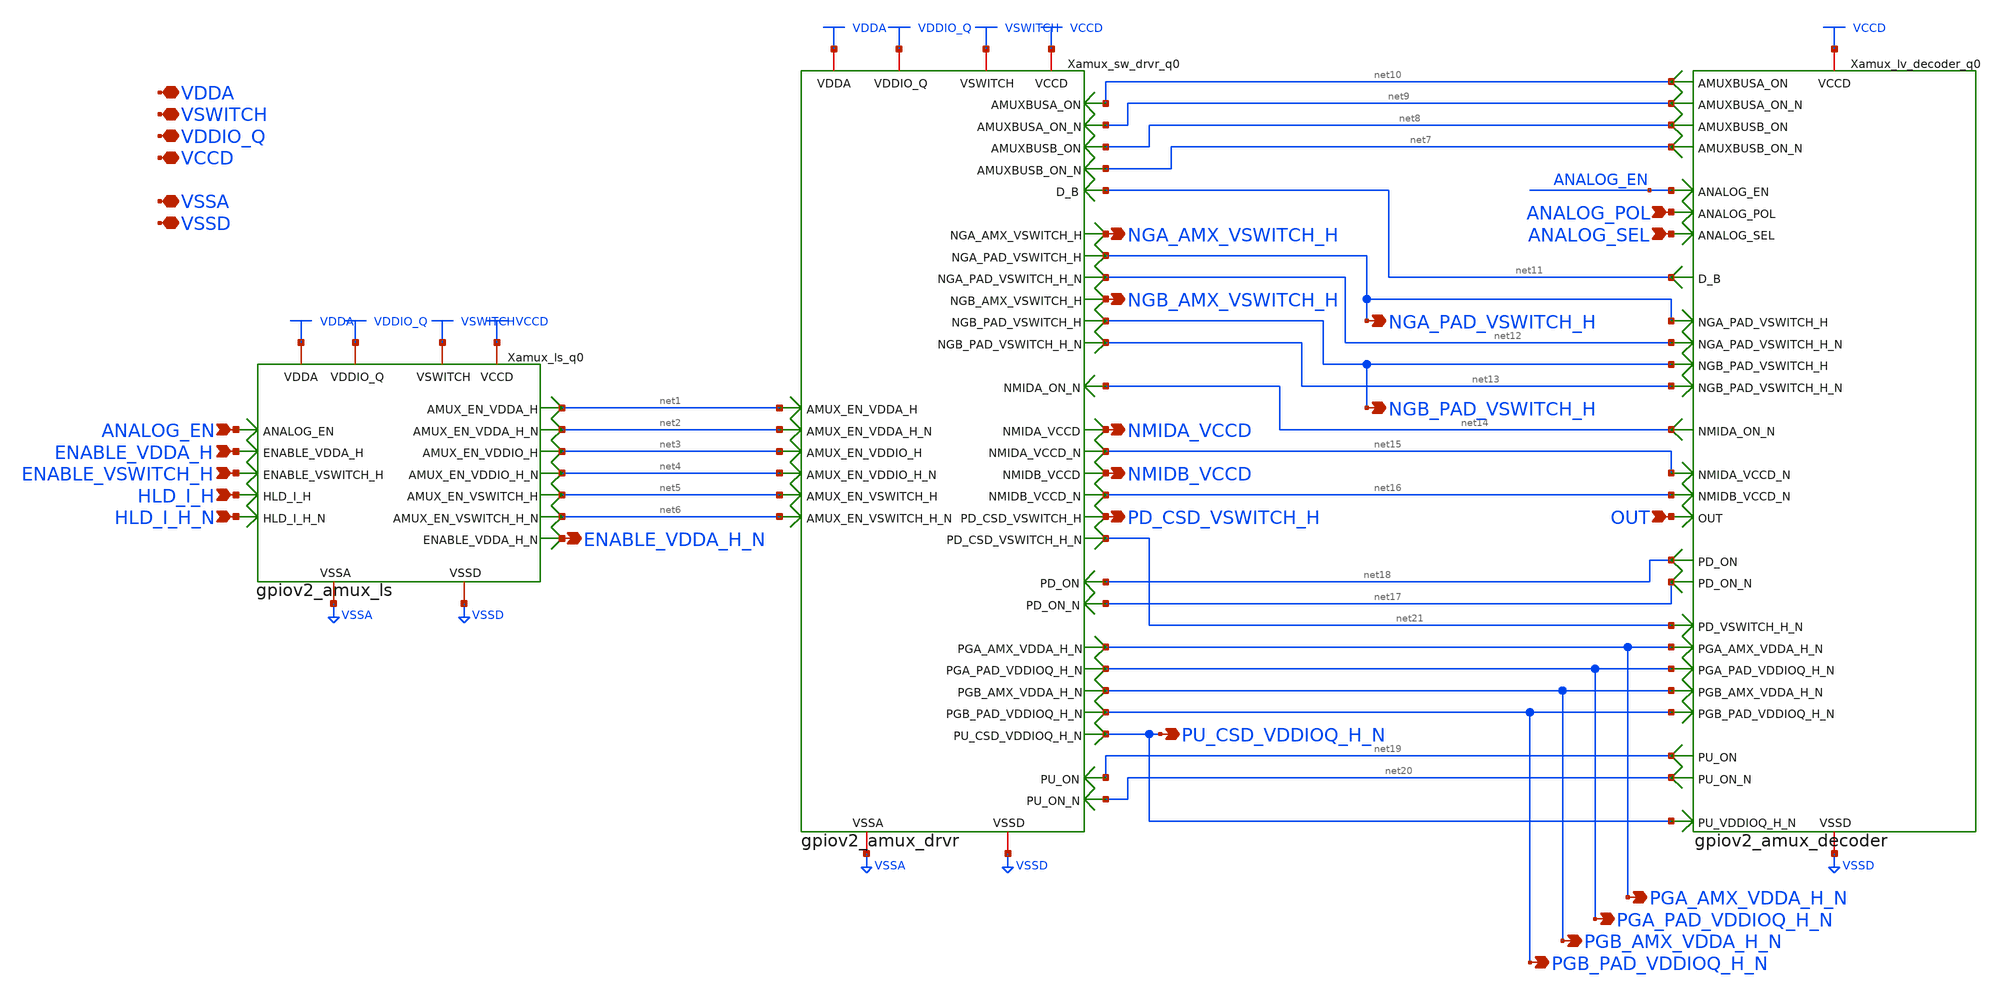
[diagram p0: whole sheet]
** sch_path: gpiov2_amux_ctl_logic.sch
* Copyright 2023 David Mitchell Bailey
* Licensed under the Apache License, Version 2.0 (the "License");
* you may not use this file except in compliance with the License.
* You may obtain a copy of the License at
* https://www.apache.org/licenses/LICENSE-2.0
* Unless required by applicable law or agreed to in writing, software
* distributed under the License is distributed on an "AS IS" BASIS,
* WITHOUT WARRANTIES OR CONDITIONS OF ANY KIND, either express or implied.
* See the License for the specific language governing permissions and
* limitations under the License.
**.subckt gpiov2_amux_ctl_logic ANALOG_EN ENABLE_VDDA_H ENABLE_VSWITCH_H HLD_I_H HLD_I_H_N
*+ ENABLE_VDDA_H_N VDDA VSWITCH VDDIO_Q VCCD VSSA VSSD ANALOG_POL ANALOG_SEL OUT NMIDA_VCCD NMIDB_VCCD
*+ PD_CSD_VSWITCH_H NGA_AMX_VSWITCH_H NGB_AMX_VSWITCH_H NGA_PAD_VSWITCH_H NGB_PAD_VSWITCH_H PU_CSD_VDDIOQ_H_N
*+ PGA_AMX_VDDA_H_N PGA_PAD_VDDIOQ_H_N PGB_AMX_VDDA_H_N PGB_PAD_VDDIOQ_H_N
*.ipin ANALOG_EN
*.ipin ENABLE_VDDA_H
*.ipin ENABLE_VSWITCH_H
*.ipin HLD_I_H
*.ipin HLD_I_H_N
*.opin ENABLE_VDDA_H_N
*.iopin VDDA
*.iopin VSWITCH
*.iopin VDDIO_Q
*.iopin VCCD
*.iopin VSSA
*.iopin VSSD
*.ipin ANALOG_POL
*.ipin ANALOG_SEL
*.ipin OUT
*.opin NMIDA_VCCD
*.opin NMIDB_VCCD
*.opin PD_CSD_VSWITCH_H
*.opin NGA_AMX_VSWITCH_H
*.opin NGB_AMX_VSWITCH_H
*.opin NGA_PAD_VSWITCH_H
*.opin NGB_PAD_VSWITCH_H
*.opin PU_CSD_VDDIOQ_H_N
*.opin PGA_AMX_VDDA_H_N
*.opin PGA_PAD_VDDIOQ_H_N
*.opin PGB_AMX_VDDA_H_N
*.opin PGB_PAD_VDDIOQ_H_N
Xamux_ls_q0 VDDA VSWITCH VDDIO_Q VCCD VSSA VSSD net1 net2 ENABLE_VDDA_H ANALOG_EN ENABLE_VDDA_H_N
+ net3 HLD_I_H net4 HLD_I_H_N net5 net6 ENABLE_VSWITCH_H gpiov2_amux_ls
Xamux_sw_drvr_q0 net11 net14 net19 net18 net17 net20 net6 net4 net3 net5 VDDA VDDIO_Q VSWITCH VCCD
+ VSSA VSSD PGA_PAD_VDDIOQ_H_N PGB_PAD_VDDIOQ_H_N net10 net8 net9 net7 PGA_AMX_VDDA_H_N PGB_AMX_VDDA_H_N
+ net2 net1 NGB_AMX_VSWITCH_H NGA_AMX_VSWITCH_H NGB_PAD_VSWITCH_H NGA_PAD_VSWITCH_H net13 net12 net16
+ net15 NMIDB_VCCD NMIDA_VCCD PD_CSD_VSWITCH_H net21 PU_CSD_VDDIOQ_H_N gpiov2_amux_drvr
Xamux_lv_decoder_q0 ANALOG_EN net9 net10 ANALOG_SEL net15 ANALOG_POL net14 NGA_PAD_VSWITCH_H
+ PGA_AMX_VDDA_H_N OUT PGA_PAD_VDDIOQ_H_N net20 PGB_PAD_VDDIOQ_H_N net12 net19 net13 PU_CSD_VDDIOQ_H_N net7 VCCD net21
+ VSSD net8 net16 net11 NGB_PAD_VSWITCH_H PGB_AMX_VDDA_H_N net17 net18 gpiov2_amux_decoder
**.ends
.end
